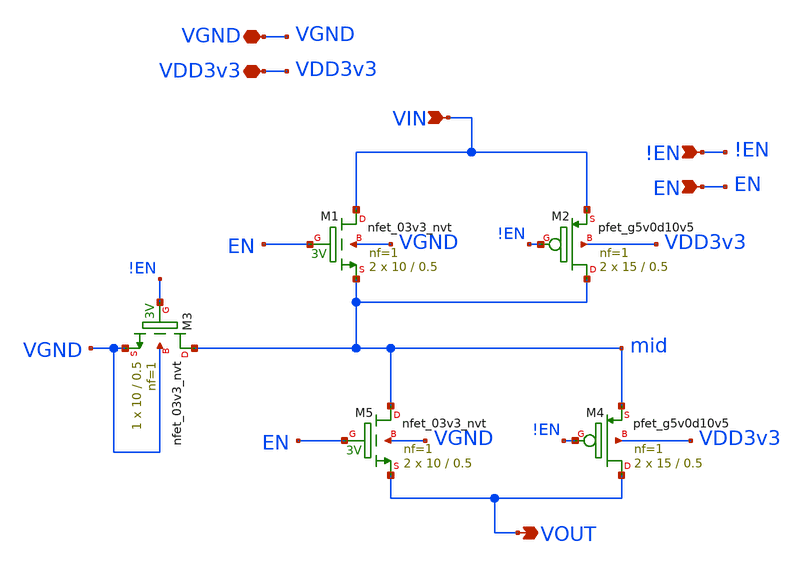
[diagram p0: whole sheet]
** sch_path: xschem/analog_mux/analogue_switch.sch
**.subckt analogue_switch EN VIN VOUT !EN VGND VDD3v3
*.ipin EN
*.ipin VIN
*.opin VOUT
*.ipin !EN
*.iopin VGND
*.iopin VDD3v3
XM2 mid !EN VIN VDD3v3 sky130_fd_pr__pfet_g5v0d10v5 L=0.5 W=15 nf=1 ad='int((nf+1)/2) * W/nf * 0.29'
+ as='int((nf+2)/2) * W/nf * 0.29' pd='2*int((nf+1)/2) * (W/nf + 0.29)' ps='2*int((nf+2)/2) * (W/nf + 0.29)'
+ nrd='0.29 / W' nrs='0.29 / W' sa=0 sb=0 sd=0 mult=2 m=2
XM1 VIN EN mid VGND sky130_fd_pr__nfet_03v3_nvt L=0.5 W=10 nf=1 ad='int((nf+1)/2) * W/nf * 0.29' as='int((nf+2)/2) * W/nf * 0.29'
+ pd='2*int((nf+1)/2) * (W/nf + 0.29)' ps='2*int((nf+2)/2) * (W/nf + 0.29)' nrd='0.29 / W' nrs='0.29 / W'
+ sa=0 sb=0 sd=0 mult=2 m=2
XM3 mid !EN VGND VGND sky130_fd_pr__nfet_03v3_nvt L=0.5 W=10 nf=1 ad='int((nf+1)/2) * W/nf * 0.29' as='int((nf+2)/2) * W/nf * 0.29'
+ pd='2*int((nf+1)/2) * (W/nf + 0.29)' ps='2*int((nf+2)/2) * (W/nf + 0.29)' nrd='0.29 / W' nrs='0.29 / W'
+ sa=0 sb=0 sd=0 mult=1 m=1
XM4 VOUT !EN mid VDD3v3 sky130_fd_pr__pfet_g5v0d10v5 L=0.5 W=15 nf=1 ad='int((nf+1)/2) * W/nf * 0.29'
+ as='int((nf+2)/2) * W/nf * 0.29' pd='2*int((nf+1)/2) * (W/nf + 0.29)' ps='2*int((nf+2)/2) * (W/nf + 0.29)'
+ nrd='0.29 / W' nrs='0.29 / W' sa=0 sb=0 sd=0 mult=2 m=2
XM5 mid EN VOUT VGND sky130_fd_pr__nfet_03v3_nvt L=0.5 W=10 nf=1 ad='int((nf+1)/2) * W/nf * 0.29' as='int((nf+2)/2) * W/nf * 0.29'
+ pd='2*int((nf+1)/2) * (W/nf + 0.29)' ps='2*int((nf+2)/2) * (W/nf + 0.29)' nrd='0.29 / W' nrs='0.29 / W'
+ sa=0 sb=0 sd=0 mult=2 m=2
**.ends
.end
